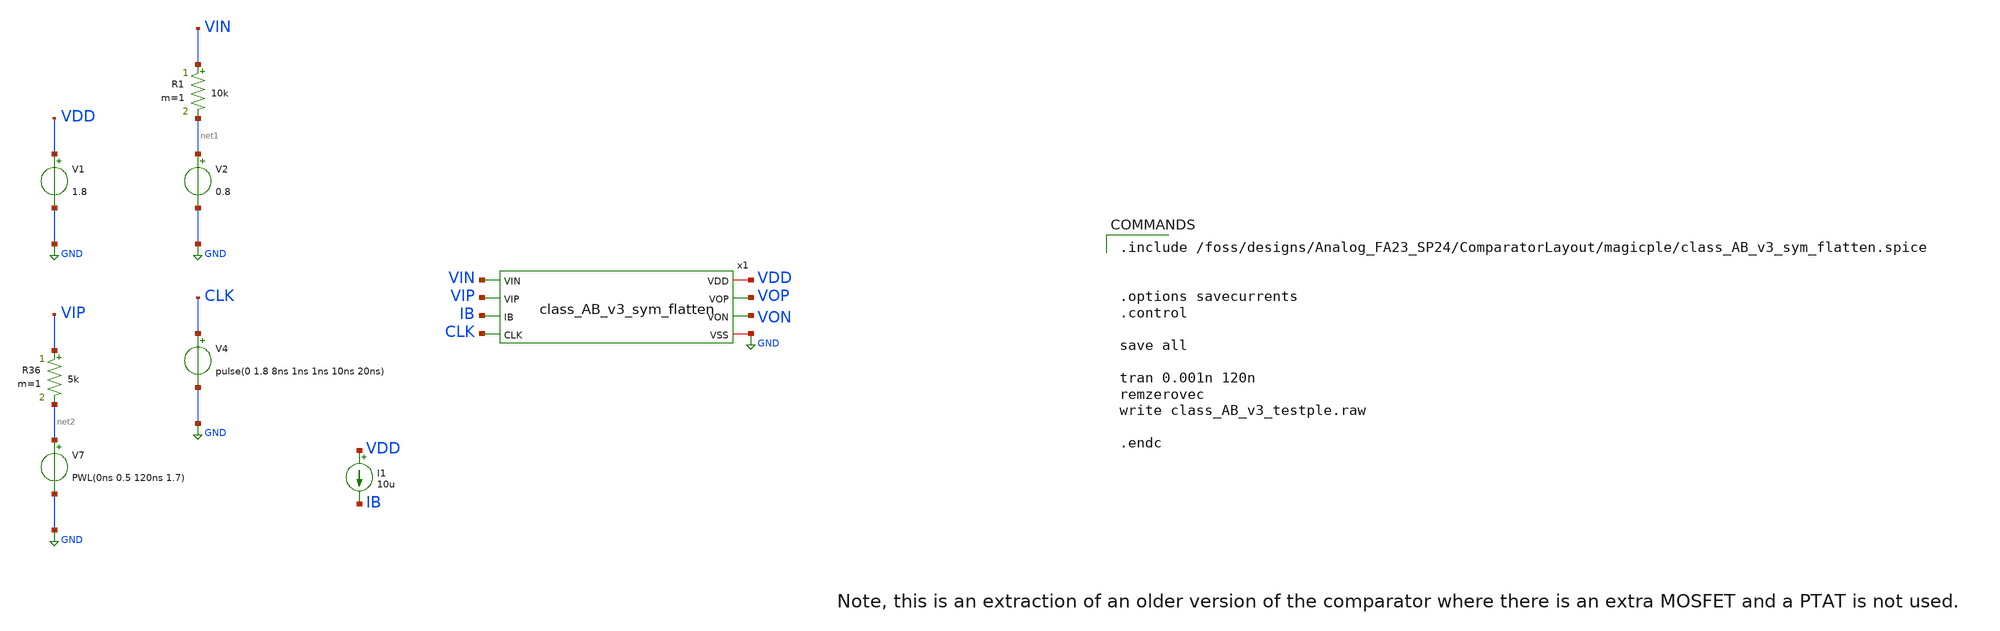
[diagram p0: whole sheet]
** sch_path: ComparatorLayout/xschem/class_AB_v3_testple.sch
.lib $::SKYWATER_MODELS/sky130.lib.spice tt
.include $::SKYWATER_STDCELLS/sky130_fd_sc_hd.spice

**.subckt class_AB_v3_testple
V1 VDD GND 1.8
V2 net1 GND 0.8
V4 CLK GND pulse(0 1.8 8ns 1ns 1ns 10ns 20ns)
R1 VIN net1 10k m=1
I1 VDD IB 10u
x1 VDD VOP VON VIN VIP IB CLK GND class_AB_v3_sym_flatten
V7 net2 GND PWL(0ns 0.5 120ns 1.7)
R36 VIP net2 5k m=1
**** begin user architecture code

.include /foss/designs/Analog_FA23_SP24/ComparatorLayout/magicple/class_AB_v3_sym_flatten.spice


.options savecurrents
.control

save all

tran 0.001n 120n
remzerovec
write class_AB_v3_testple.raw

.endc


**** end user architecture code
**.ends
.GLOBAL GND
.end
